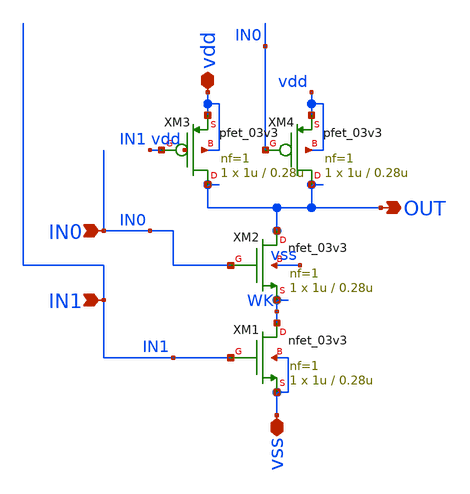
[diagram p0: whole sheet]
** sch_path: schematics/PC/NAND2/NAND2.sch
**.subckt NAND2 vdd vss OUT IN0 IN1
*.iopin vdd
*.iopin vss
*.opin OUT
*.ipin IN0
*.ipin IN1
XM1 WK IN1 vss vss nfet_03v3 L=0.28u W=1u nf=1 ad='int((nf+1)/2) * W/nf * 0.18u' as='int((nf+2)/2) * W/nf * 0.18u'
+ pd='2*int((nf+1)/2) * (W/nf + 0.18u)' ps='2*int((nf+2)/2) * (W/nf + 0.18u)' nrd='0.18u / W' nrs='0.18u / W'
+ sa=0 sb=0 sd=0 m=1
XM2 OUT IN0 WK vss nfet_03v3 L=0.28u W=1u nf=1 ad='int((nf+1)/2) * W/nf * 0.18u' as='int((nf+2)/2) * W/nf * 0.18u'
+ pd='2*int((nf+1)/2) * (W/nf + 0.18u)' ps='2*int((nf+2)/2) * (W/nf + 0.18u)' nrd='0.18u / W' nrs='0.18u / W'
+ sa=0 sb=0 sd=0 m=1
XM3 OUT IN1 vdd vdd pfet_03v3 L=0.28u W=1u nf=1 ad='int((nf+1)/2) * W/nf * 0.18u' as='int((nf+2)/2) * W/nf * 0.18u'
+ pd='2*int((nf+1)/2) * (W/nf + 0.18u)' ps='2*int((nf+2)/2) * (W/nf + 0.18u)' nrd='0.18u / W' nrs='0.18u / W'
+ sa=0 sb=0 sd=0 m=1
XM4 OUT IN0 vdd vdd pfet_03v3 L=0.28u W=1u nf=1 ad='int((nf+1)/2) * W/nf * 0.18u' as='int((nf+2)/2) * W/nf * 0.18u'
+ pd='2*int((nf+1)/2) * (W/nf + 0.18u)' ps='2*int((nf+2)/2) * (W/nf + 0.18u)' nrd='0.18u / W' nrs='0.18u / W'
+ sa=0 sb=0 sd=0 m=1
**.ends
.end
